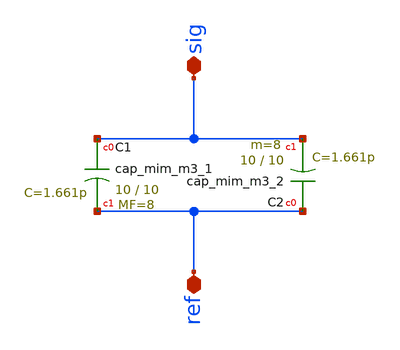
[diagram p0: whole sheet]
** sch_path: xschem/Switched_Caps/mim_cap_stacked_3pF.sch
**.subckt mim_cap_stacked_3pF sig ref
*.iopin sig
*.iopin ref
XC1 sig ref sky130_fd_pr__cap_mim_m3_1 W=10 L=10 MF=8 m=8
XC2 ref sig sky130_fd_pr__cap_mim_m3_2 W=10 L=10 MF=8 m=8
**.ends
.end
